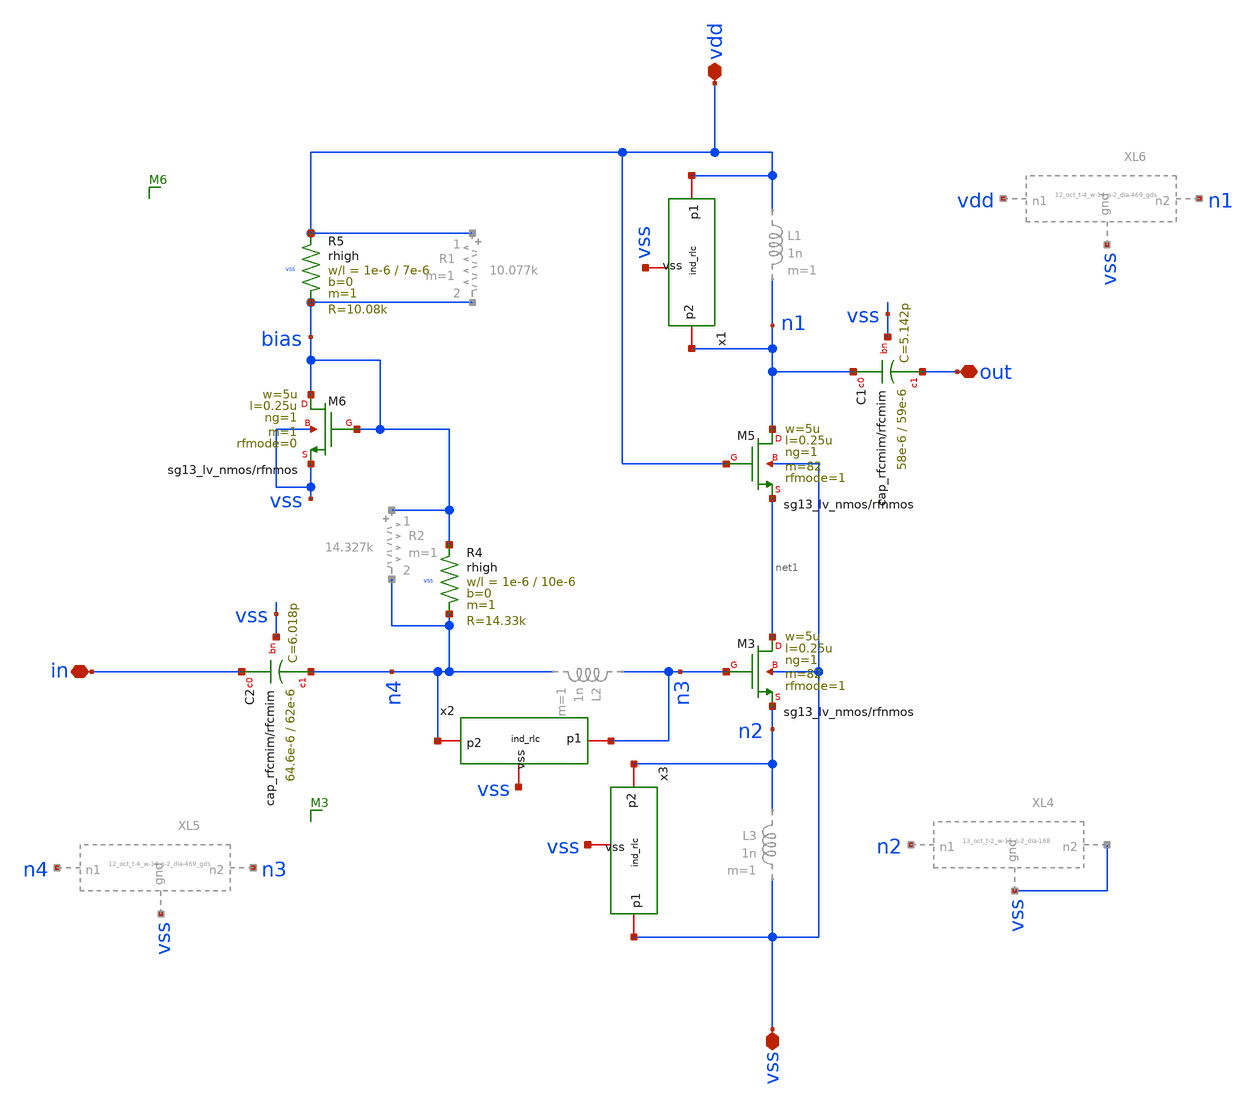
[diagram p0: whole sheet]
** sch_path: LNA7096-main/schematic/xschem/01_lna/LNA_no_buff_rlc.sch
**.subckt LNA_no_buff_rlc vdd vss in out
*.iopin vdd
*.iopin vss
*.iopin in
*.iopin out
XR4 bias n4 vss rhigh w=1e-6 l=10e-6 m=1 b=0 mm_ok=1
XR5 vdd bias vss rhigh w=1e-6 l=7e-6 m=1 b=0 mm_ok=1
XC1 n1 out vss cap_rfcmim w=58e-6 l=59e-6 wfeed=5.0e-6 m=1 mm_ok=1
XM3 net1 n3 n2 vss sg13_lv_nmos w=5u l=0.25u ng=1 m=82 rfmode=1 mm_ok=1
XM5 n1 vdd net1 vss sg13_lv_nmos w=5u l=0.25u ng=1 m=82 rfmode=1 mm_ok=1
XM6 bias bias vss vss sg13_lv_nmos w=5u l=0.25u ng=1 m=1 rfmode=0 mm_ok=1
XC2 in n4 vss cap_rfcmim w=64.6e-6 l=62e-6 wfeed=5.0e-6 m=1 mm_ok=1
x1 n1 vdd vss ind_rlc Lser=18.1n Rser=9.8 Cshunt1=61.6f Rshunt1=2696 Cshunt2=62.2f Rshunt2=2774
x3 n2 vss vss ind_rlc Lser=1.381n Rser=1.339 Cshunt1=37f Rshunt1=2401 Cshunt2=38.5f Rshunt2=2353
x2 n4 n3 vss ind_rlc Lser=18.1n Rser=9.8 Cshunt1=61.6f Rshunt1=2696 Cshunt2=62.2f Rshunt2=2774
**.ends

* expanding   symbol:  01_lna/13_oct_t-2_w-15_s-2_dia-168.sym # of pins=3
** sym_path: LNA7096-main/schematic/xschem/01_lna/ind_lg.sym
.include /home/ic_design_trg/lna_ihp/xschem/01_lna/lna_pads/simulation/ngspice_s2p/13_oct_t-2_w-15_s-2_dia-168.inc

* expanding   symbol:  01_lna/12_oct_t-4_w-14_s-2_dia-469_gds.sym # of pins=3
** sym_path: LNA7096-main/schematic/xschem/01_lna/ind_lg.sym
.include /home/ic_design_trg/lna_ihp/xschem/01_lna/lna_pads/simulation/ngspice_s2p/12_oct_t-4_w-14_s-2_dia-469_gds.inc

* expanding   symbol:  01_lna/ind_rlc.sym # of pins=3
** sym_path: LNA7096-main/schematic/xschem/01_lna/ind_rlc.sym
** sch_path: LNA7096-main/schematic/xschem/01_lna/ind_rlc.sch
.subckt ind_rlc p2 p1 vss  Lser=1n Rser=1k Rshunt1=1k Cshunt1=2p Rshunt2=1k Cshunt2=2p
*.iopin p1
*.iopin p2
*.iopin vss
L1 net2 p1 'Lser' m=1
R1 net2 p2 'Rser' m=1
R2 p1 net1 'Rshunt1' m=1
C1 net1 vss 'Cshunt1' m=1
R5 p2 net3 'Rshunt2' m=1
C4 net3 vss 'Cshunt2' m=1
.ends

.end
